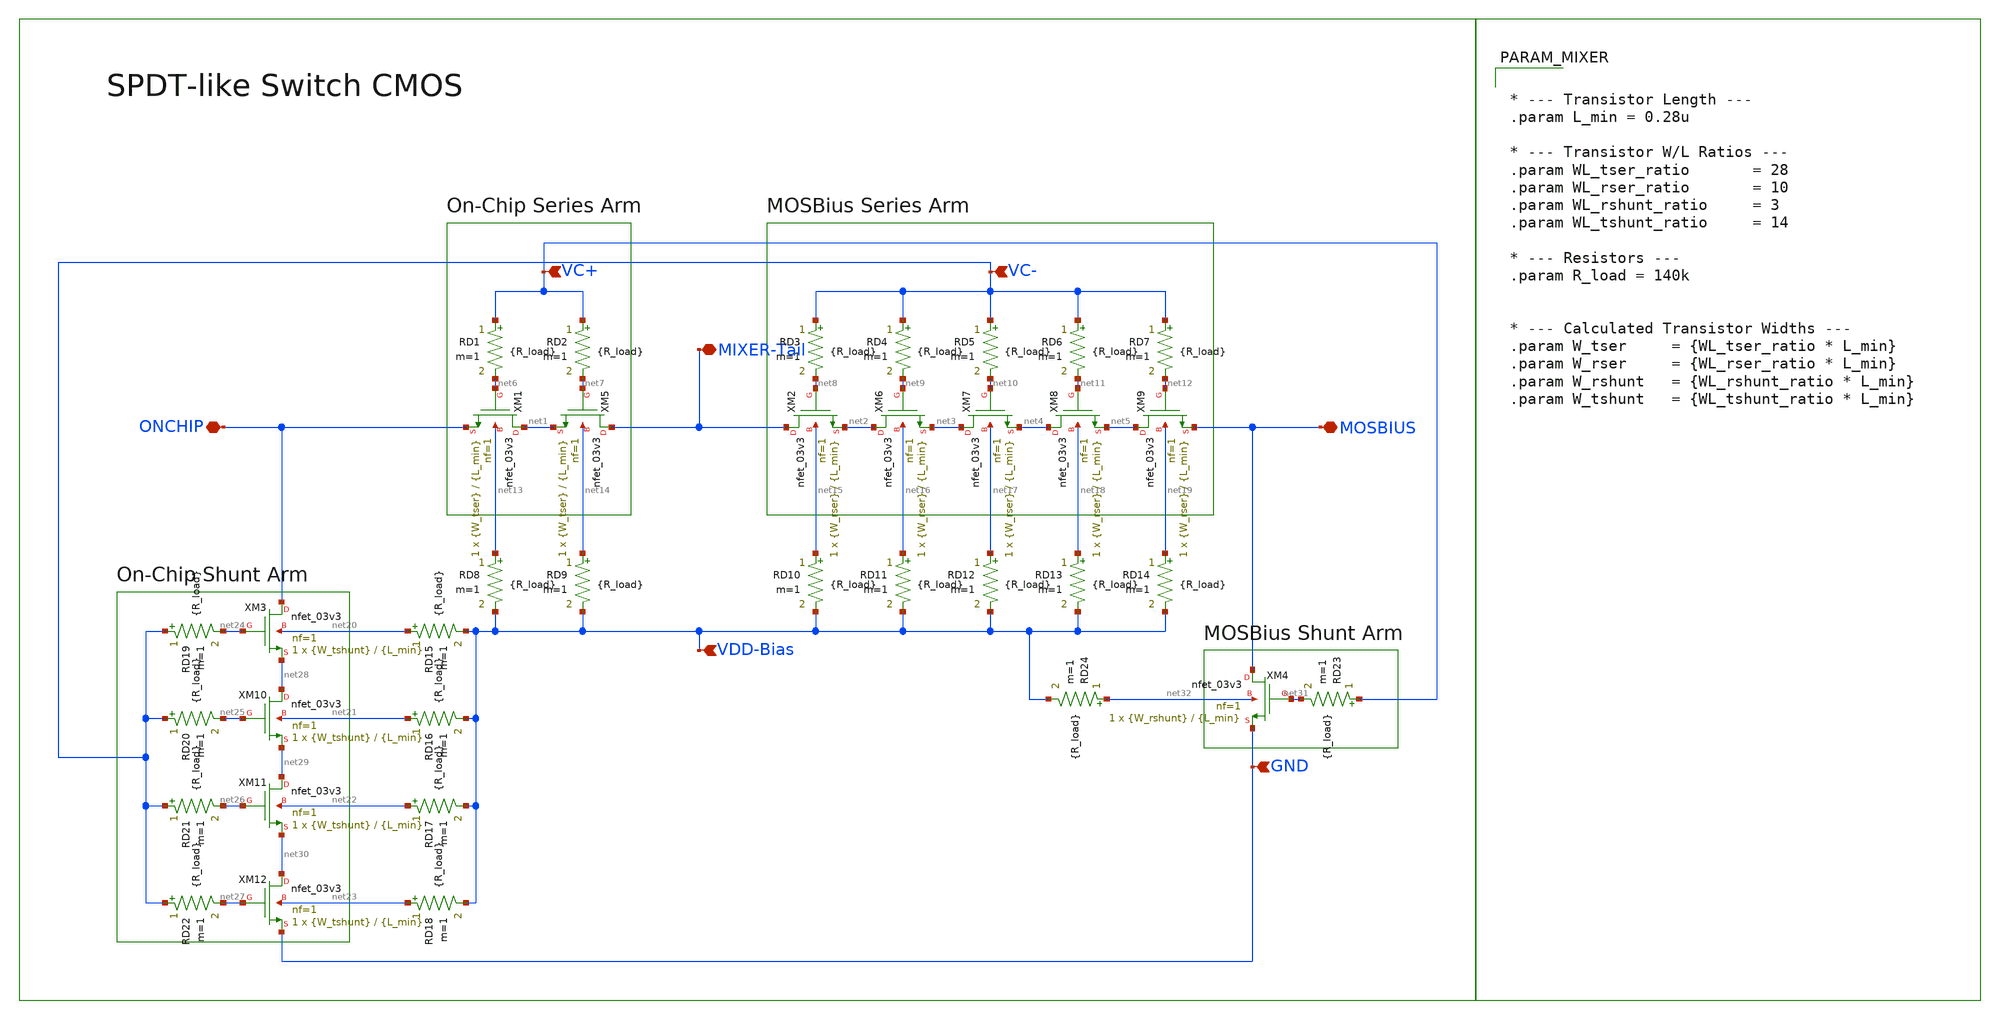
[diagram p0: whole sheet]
** sch_path: Project/1-on-chip/schematic/Mixer/Switch.sch
**.subckt Switch MIXER-Tail ONCHIP MOSBIUS VDD-Bias GND VC+ VC-
*.iopin MIXER-Tail
*.iopin ONCHIP
*.iopin MOSBIUS
*.ipin VDD-Bias
*.ipin GND
*.ipin VC+
*.ipin VC-
XM1 net1 net6 ONCHIP net13 nfet_03v3 L={L_min} W={W_tser} nf=1 ad='int((nf+1)/2) * W/nf * 0.18u' as='int((nf+2)/2) * W/nf * 0.18u'
+ pd='2*int((nf+1)/2) * (W/nf + 0.18u)' ps='2*int((nf+2)/2) * (W/nf + 0.18u)' nrd='0.18u / W' nrs='0.18u / W'
+ sa=0 sb=0 sd=0 m=1
XM2 MIXER-Tail net8 net2 net15 nfet_03v3 L={L_min} W={W_rser} nf=1 ad='int((nf+1)/2) * W/nf * 0.18u'
+ as='int((nf+2)/2) * W/nf * 0.18u' pd='2*int((nf+1)/2) * (W/nf + 0.18u)' ps='2*int((nf+2)/2) * (W/nf + 0.18u)'
+ nrd='0.18u / W' nrs='0.18u / W' sa=0 sb=0 sd=0 m=1
XM3 ONCHIP net24 net28 net20 nfet_03v3 L={L_min} W={W_tshunt} nf=1 ad='int((nf+1)/2) * W/nf * 0.18u'
+ as='int((nf+2)/2) * W/nf * 0.18u' pd='2*int((nf+1)/2) * (W/nf + 0.18u)' ps='2*int((nf+2)/2) * (W/nf + 0.18u)'
+ nrd='0.18u / W' nrs='0.18u / W' sa=0 sb=0 sd=0 m=1
XM4 MOSBIUS net31 GND net32 nfet_03v3 L={L_min} W={W_rshunt} nf=1 ad='int((nf+1)/2) * W/nf * 0.18u' as='int((nf+2)/2) * W/nf * 0.18u'
+ pd='2*int((nf+1)/2) * (W/nf + 0.18u)' ps='2*int((nf+2)/2) * (W/nf + 0.18u)' nrd='0.18u / W' nrs='0.18u / W'
+ sa=0 sb=0 sd=0 m=1
XM5 MIXER-Tail net7 net1 net14 nfet_03v3 L={L_min} W={W_tser} nf=1 ad='int((nf+1)/2) * W/nf * 0.18u'
+ as='int((nf+2)/2) * W/nf * 0.18u' pd='2*int((nf+1)/2) * (W/nf + 0.18u)' ps='2*int((nf+2)/2) * (W/nf + 0.18u)'
+ nrd='0.18u / W' nrs='0.18u / W' sa=0 sb=0 sd=0 m=1
RD1 VC+ net6 {R_load} m=1
RD2 VC+ net7 {R_load} m=1
RD3 VC- net8 {R_load} m=1
RD4 VC- net9 {R_load} m=1
RD5 VC- net10 {R_load} m=1
RD6 VC- net11 {R_load} m=1
RD7 VC- net12 {R_load} m=1
RD8 net13 VDD-Bias {R_load} m=1
RD9 net14 VDD-Bias {R_load} m=1
RD10 net15 VDD-Bias {R_load} m=1
RD11 net16 VDD-Bias {R_load} m=1
RD12 net17 VDD-Bias {R_load} m=1
RD13 net18 VDD-Bias {R_load} m=1
RD14 net19 VDD-Bias {R_load} m=1
RD15 net20 VDD-Bias {R_load} m=1
RD16 net21 VDD-Bias {R_load} m=1
RD17 net22 VDD-Bias {R_load} m=1
RD18 net23 VDD-Bias {R_load} m=1
RD19 VC- net24 {R_load} m=1
RD20 VC- net25 {R_load} m=1
RD21 VC- net26 {R_load} m=1
RD22 VC- net27 {R_load} m=1
XM6 net2 net9 net3 net16 nfet_03v3 L={L_min} W={W_rser} nf=1 ad='int((nf+1)/2) * W/nf * 0.18u' as='int((nf+2)/2) * W/nf * 0.18u'
+ pd='2*int((nf+1)/2) * (W/nf + 0.18u)' ps='2*int((nf+2)/2) * (W/nf + 0.18u)' nrd='0.18u / W' nrs='0.18u / W'
+ sa=0 sb=0 sd=0 m=1
XM7 net3 net10 net4 net17 nfet_03v3 L={L_min} W={W_rser} nf=1 ad='int((nf+1)/2) * W/nf * 0.18u' as='int((nf+2)/2) * W/nf * 0.18u'
+ pd='2*int((nf+1)/2) * (W/nf + 0.18u)' ps='2*int((nf+2)/2) * (W/nf + 0.18u)' nrd='0.18u / W' nrs='0.18u / W'
+ sa=0 sb=0 sd=0 m=1
XM8 net4 net11 net5 net18 nfet_03v3 L={L_min} W={W_rser} nf=1 ad='int((nf+1)/2) * W/nf * 0.18u' as='int((nf+2)/2) * W/nf * 0.18u'
+ pd='2*int((nf+1)/2) * (W/nf + 0.18u)' ps='2*int((nf+2)/2) * (W/nf + 0.18u)' nrd='0.18u / W' nrs='0.18u / W'
+ sa=0 sb=0 sd=0 m=1
XM9 net5 net12 MOSBIUS net19 nfet_03v3 L={L_min} W={W_rser} nf=1 ad='int((nf+1)/2) * W/nf * 0.18u' as='int((nf+2)/2) * W/nf * 0.18u'
+ pd='2*int((nf+1)/2) * (W/nf + 0.18u)' ps='2*int((nf+2)/2) * (W/nf + 0.18u)' nrd='0.18u / W' nrs='0.18u / W'
+ sa=0 sb=0 sd=0 m=1
RD23 VC+ net31 {R_load} m=1
XM10 net28 net25 net29 net21 nfet_03v3 L={L_min} W={W_tshunt} nf=1 ad='int((nf+1)/2) * W/nf * 0.18u'
+ as='int((nf+2)/2) * W/nf * 0.18u' pd='2*int((nf+1)/2) * (W/nf + 0.18u)' ps='2*int((nf+2)/2) * (W/nf + 0.18u)'
+ nrd='0.18u / W' nrs='0.18u / W' sa=0 sb=0 sd=0 m=1
XM11 net29 net26 net30 net22 nfet_03v3 L={L_min} W={W_tshunt} nf=1 ad='int((nf+1)/2) * W/nf * 0.18u'
+ as='int((nf+2)/2) * W/nf * 0.18u' pd='2*int((nf+1)/2) * (W/nf + 0.18u)' ps='2*int((nf+2)/2) * (W/nf + 0.18u)'
+ nrd='0.18u / W' nrs='0.18u / W' sa=0 sb=0 sd=0 m=1
XM12 net30 net27 GND net23 nfet_03v3 L={L_min} W={W_tshunt} nf=1 ad='int((nf+1)/2) * W/nf * 0.18u' as='int((nf+2)/2) * W/nf * 0.18u'
+ pd='2*int((nf+1)/2) * (W/nf + 0.18u)' ps='2*int((nf+2)/2) * (W/nf + 0.18u)' nrd='0.18u / W' nrs='0.18u / W'
+ sa=0 sb=0 sd=0 m=1
RD24 net32 VDD-Bias {R_load} m=1
**** begin user architecture code


* --- Transistor Length ---
.param L_min = 0.28u

* --- Transistor W/L Ratios ---
.param WL_tser_ratio       = 28
.param WL_rser_ratio       = 10
.param WL_rshunt_ratio     = 3
.param WL_tshunt_ratio     = 14

* --- Resistors ---
.param R_load = 140k


* --- Calculated Transistor Widths ---
.param W_tser     = {WL_tser_ratio * L_min}
.param W_rser     = {WL_rser_ratio * L_min}
.param W_rshunt   = {WL_rshunt_ratio * L_min}
.param W_tshunt   = {WL_tshunt_ratio * L_min}


**** end user architecture code
**.ends
.end
